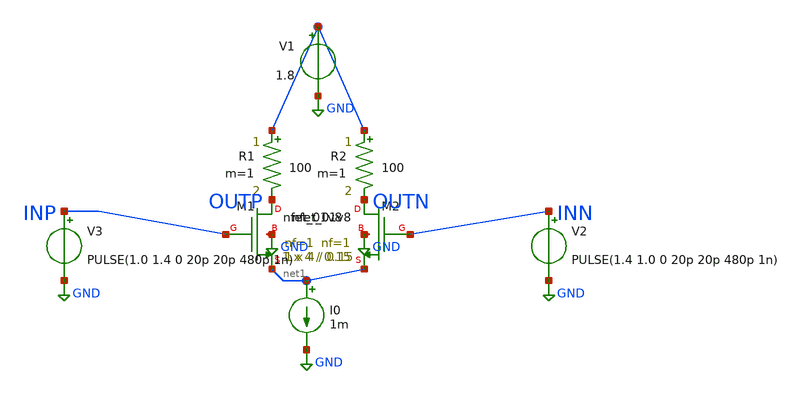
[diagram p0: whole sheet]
** sch_path: analog/tx_driver.sch
**.subckt tx_driver
XM1 OUTP INP net1 GND sky130_fd_pr__nfet_01v8 L=0.15 W=4 nf=1 ad='int((1 + 1)/2) * 4 / 1 * 0.29' as='int((1 + 2)/2) * 4 / 1 * 0.29'
+ pd='2*int((1 + 1)/2) * (4 / 1 + 0.29)' ps='2*int((1 + 2)/2) * (4 / 1 + 0.29)' nrd='0.29 / 4 ' nrs='0.29 / 4 '
+ sa=0 sb=0 sd=0 mult=1 m=1
XM2 OUTN INN net1 GND sky130_fd_pr__nfet_01v8 L=0.15 W=4 nf=1 ad='int((1 + 1)/2) * 4 / 1 * 0.29' as='int((1 + 2)/2) * 4 / 1 * 0.29'
+ pd='2*int((1 + 1)/2) * (4 / 1 + 0.29)' ps='2*int((1 + 2)/2) * (4 / 1 + 0.29)' nrd='0.29 / 4 ' nrs='0.29 / 4 '
+ sa=0 sb=0 sd=0 mult=1 m=1
R1 net2 OUTP 100 m=1
R2 net2 OUTN 100 m=1
I0 net1 GND 1m
V1 net2 GND 1.8
V2 INN GND PULSE(1.4 1.0 0 20p 20p 480p 1n)
V3 INP GND PULSE(1.0 1.4 0 20p 20p 480p 1n)
**.ends
.GLOBAL GND
.end
